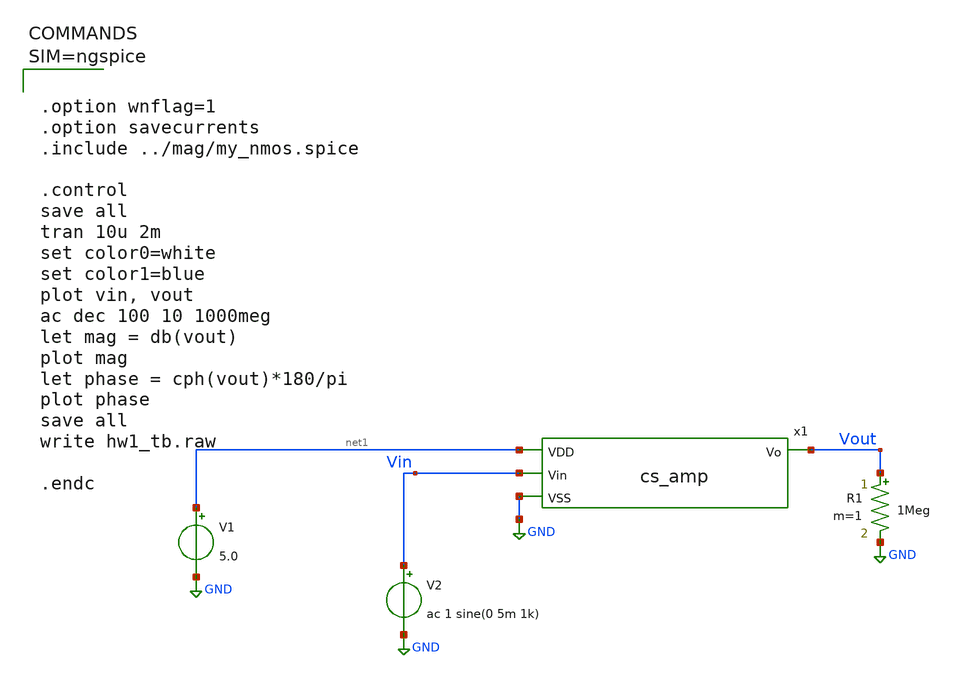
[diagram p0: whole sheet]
** sch_path: hw02/xschem/amp_tb.sch
**.subckt amp_tb
V1 net1 GND 5.0
V2 Vin GND ac 1 sine(0 5m 1k)
x1 net1 Vout Vin GND cs_amp
R1 Vout GND 1Meg m=1
**** begin user architecture code



.option wnflag=1
.option savecurrents
.include ../mag/my_nmos.spice

.control
save all
tran 10u 2m
set color0=white
set color1=blue
plot vin, vout
ac dec 100 10 1000meg
let mag = db(vout)
plot mag
let phase = cph(vout)*180/pi
plot phase
save all
write hw1_tb.raw

.endc




** opencircuitdesign pdks install
.lib $::SKYWATER_MODELS/sky130.lib.spice tt


**** end user architecture code
**.ends
.GLOBAL GND
.end
